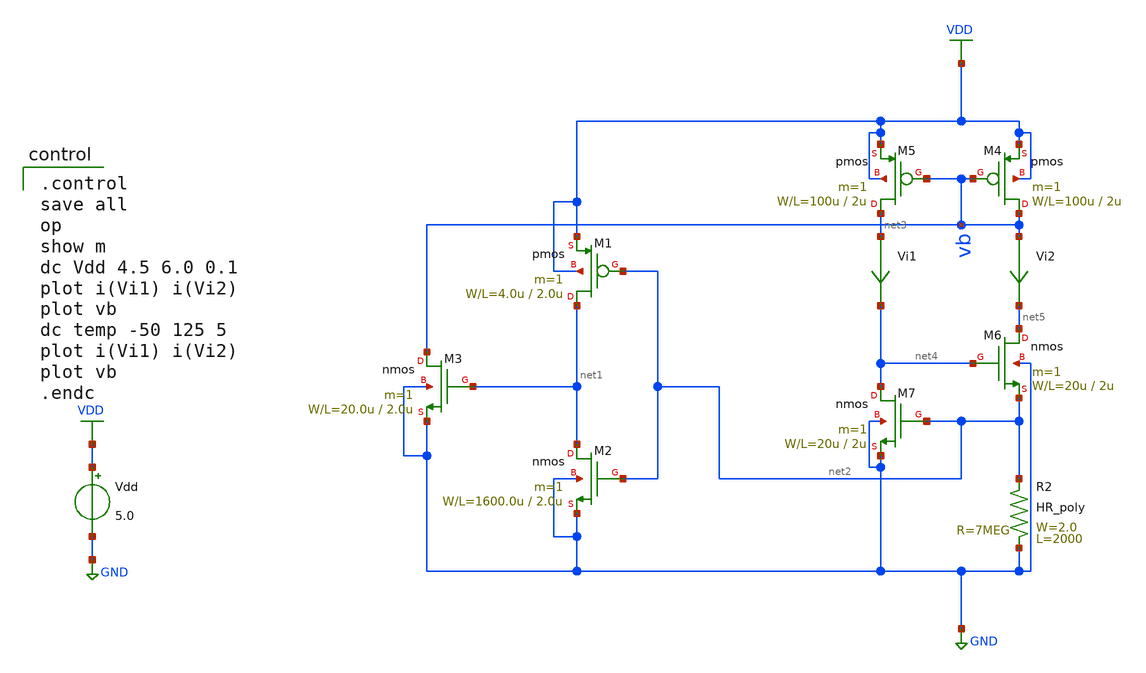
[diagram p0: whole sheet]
** sch_path: OR1/PTC06/current-source/cs_startup_usage_tb.sch
**.subckt cs_startup_usage_tb
M1 net1 net2 VDD VDD pmos L=2.0u W=4.0u m=1
M2 net1 net2 GND GND nmos L=2.0u W=1600.0u m=1
M3 vb net1 GND GND nmos L=2.0u W=20.0u m=1
R2 GND net2 HR_poly W=2.0 L=2000
M4 vb vb VDD VDD pmos L=2u W=100u m=1
M5 net3 vb VDD VDD pmos L=2u W=100u m=1
M6 net5 net4 net2 GND nmos L=2u W=20u m=1
M7 net4 net2 GND GND nmos L=2u W=20u m=1
Vdd VDD GND 5.0
Vi1 net3 net4 0
.save i(vi1)
Vi2 vb net5 0
.save i(vi2)
**** begin user architecture code

.control
save all
op
show m
dc Vdd 4.5 6.0 0.1
plot i(Vi1) i(Vi2)
plot vb
dc temp -50 125 5
plot i(Vi1) i(Vi2)
plot vb
.endc

 .include $::LIB/mos.lib
.include $::LIB/passive.lib
.include $::LIB/diode.lib
**** end user architecture code
**.ends
.GLOBAL VDD
.GLOBAL GND
.end
